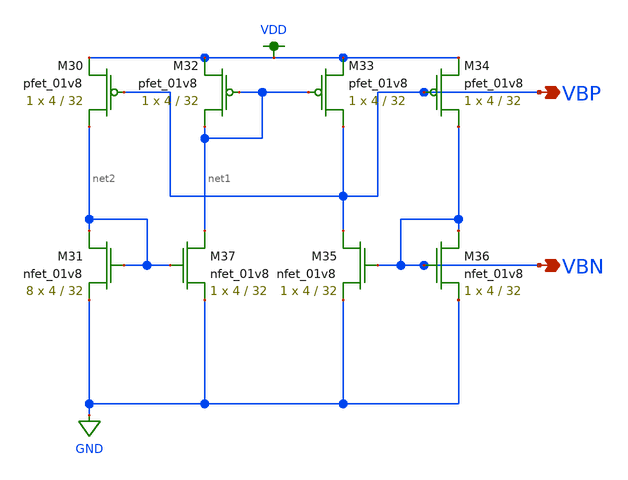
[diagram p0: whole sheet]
** sch_path: schemas/biasGen.sch
**.subckt biasGen VBN VBP
*.opin VBN
*.opin VBP
XM30 net2 VBP VDD VDD sky130_fd_pr__pfet_01v8 L=32 W=4 nf=1 ad='int((nf+1)/2) * W/nf * 0.29' as='int((nf+2)/2) * W/nf * 0.29'
+ pd='2*int((nf+1)/2) * (W/nf + 0.29)' ps='2*int((nf+2)/2) * (W/nf + 0.29)' nrd='0.29 / W' nrs='0.29 / W'
+ sa=0 sb=0 sd=0 mult=1 m=1
XM31 net2 net2 GND GND sky130_fd_pr__nfet_01v8 L=32 W=4 nf=1 ad='int((nf+1)/2) * W/nf * 0.29' as='int((nf+2)/2) * W/nf * 0.29'
+ pd='2*int((nf+1)/2) * (W/nf + 0.29)' ps='2*int((nf+2)/2) * (W/nf + 0.29)' nrd='0.29 / W' nrs='0.29 / W'
+ sa=0 sb=0 sd=0 mult=8 m=8
XM32 net1 net1 VDD VDD sky130_fd_pr__pfet_01v8 L=32 W=4 nf=1 ad='int((nf+1)/2) * W/nf * 0.29' as='int((nf+2)/2) * W/nf * 0.29'
+ pd='2*int((nf+1)/2) * (W/nf + 0.29)' ps='2*int((nf+2)/2) * (W/nf + 0.29)' nrd='0.29 / W' nrs='0.29 / W'
+ sa=0 sb=0 sd=0 mult=1 m=1
XM33 VBP net1 VDD VDD sky130_fd_pr__pfet_01v8 L=32 W=4 nf=1 ad='int((nf+1)/2) * W/nf * 0.29' as='int((nf+2)/2) * W/nf * 0.29'
+ pd='2*int((nf+1)/2) * (W/nf + 0.29)' ps='2*int((nf+2)/2) * (W/nf + 0.29)' nrd='0.29 / W' nrs='0.29 / W'
+ sa=0 sb=0 sd=0 mult=1 m=1
XM34 VBN VBP VDD VDD sky130_fd_pr__pfet_01v8 L=32 W=4 nf=1 ad='int((nf+1)/2) * W/nf * 0.29' as='int((nf+2)/2) * W/nf * 0.29'
+ pd='2*int((nf+1)/2) * (W/nf + 0.29)' ps='2*int((nf+2)/2) * (W/nf + 0.29)' nrd='0.29 / W' nrs='0.29 / W'
+ sa=0 sb=0 sd=0 mult=1 m=1
XM35 VBP VBN GND GND sky130_fd_pr__nfet_01v8 L=32 W=4 nf=1 ad='int((nf+1)/2) * W/nf * 0.29' as='int((nf+2)/2) * W/nf * 0.29'
+ pd='2*int((nf+1)/2) * (W/nf + 0.29)' ps='2*int((nf+2)/2) * (W/nf + 0.29)' nrd='0.29 / W' nrs='0.29 / W'
+ sa=0 sb=0 sd=0 mult=1 m=1
XM36 VBN VBN GND GND sky130_fd_pr__nfet_01v8 L=32 W=4 nf=1 ad='int((nf+1)/2) * W/nf * 0.29' as='int((nf+2)/2) * W/nf * 0.29'
+ pd='2*int((nf+1)/2) * (W/nf + 0.29)' ps='2*int((nf+2)/2) * (W/nf + 0.29)' nrd='0.29 / W' nrs='0.29 / W'
+ sa=0 sb=0 sd=0 mult=1 m=1
XM37 net1 net2 GND GND sky130_fd_pr__nfet_01v8 L=32 W=4 nf=1 ad='int((nf+1)/2) * W/nf * 0.29' as='int((nf+2)/2) * W/nf * 0.29'
+ pd='2*int((nf+1)/2) * (W/nf + 0.29)' ps='2*int((nf+2)/2) * (W/nf + 0.29)' nrd='0.29 / W' nrs='0.29 / W'
+ sa=0 sb=0 sd=0 mult=1 m=1
**.ends
.GLOBAL GND
.GLOBAL VDD
.end
